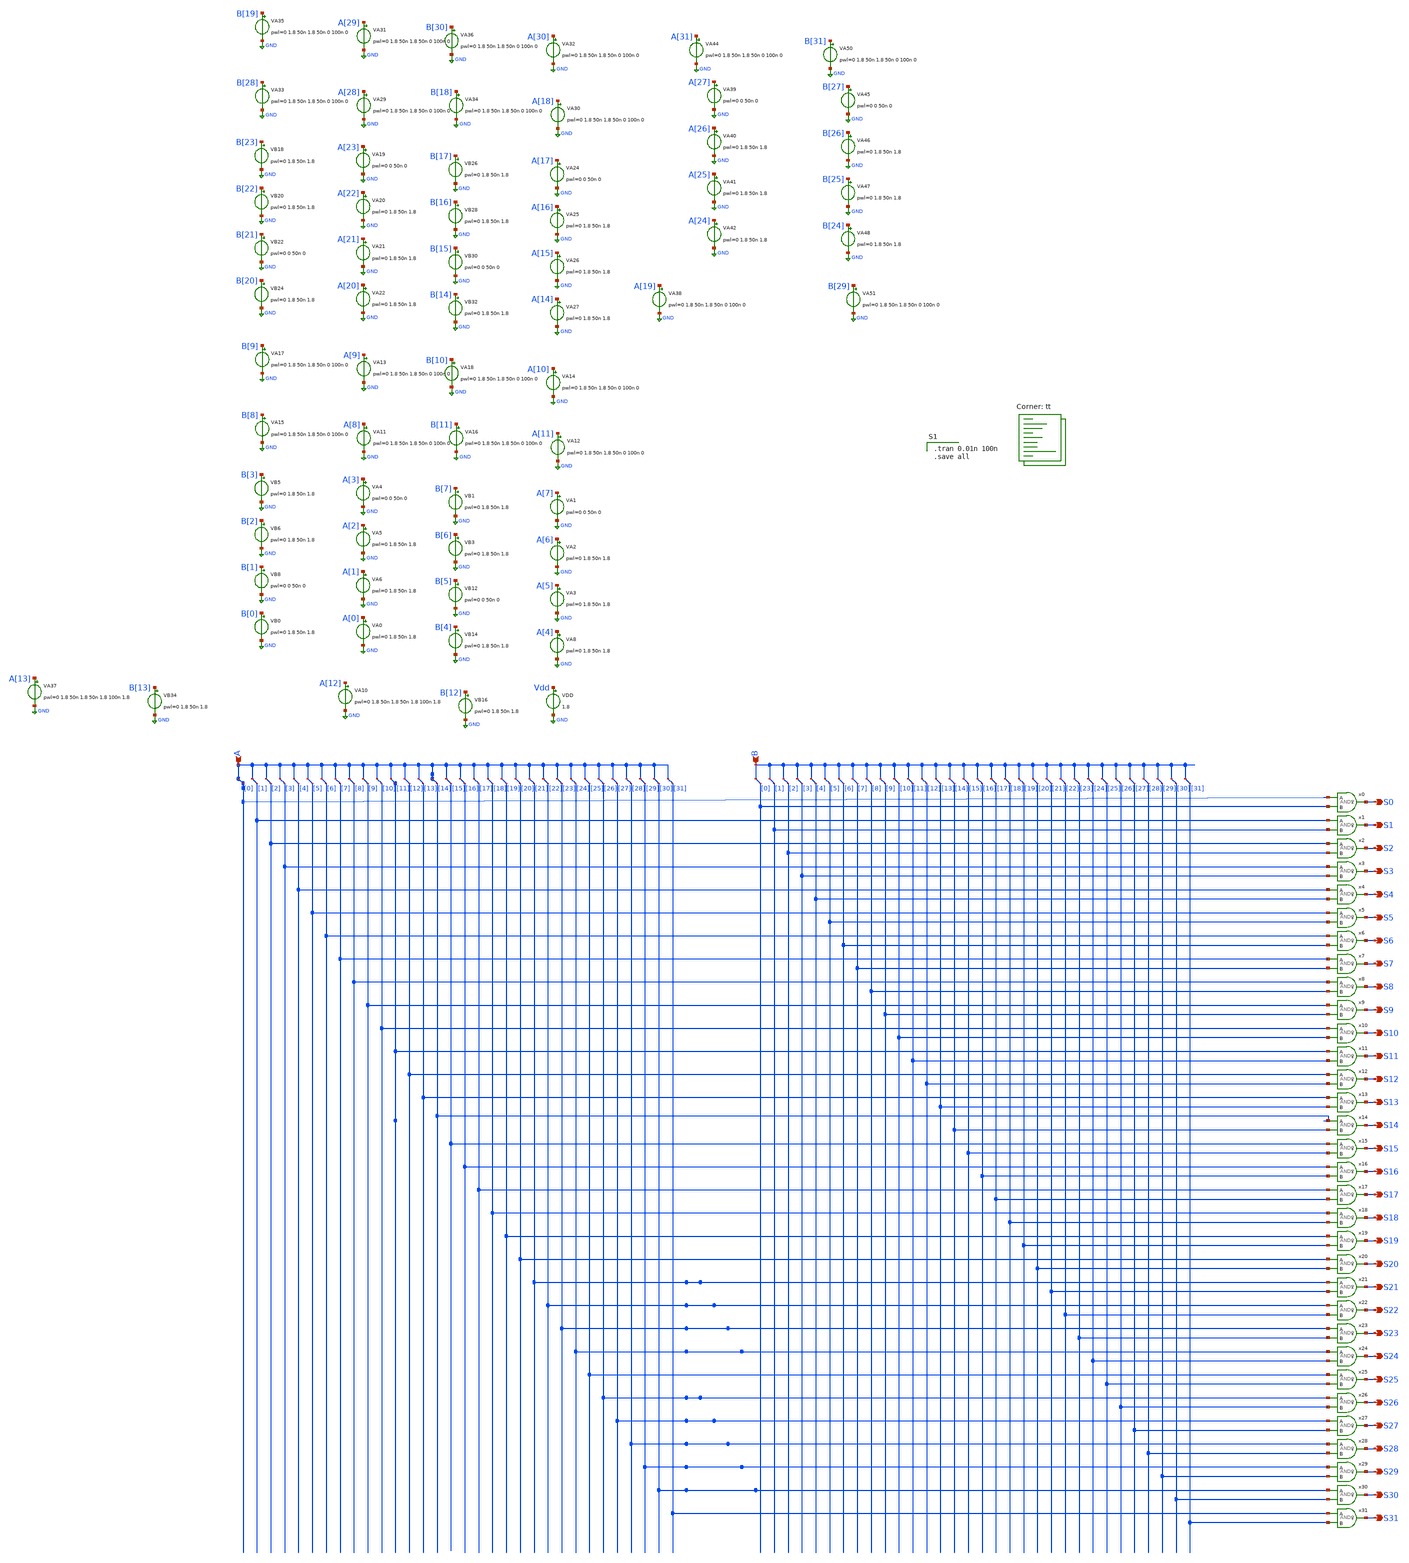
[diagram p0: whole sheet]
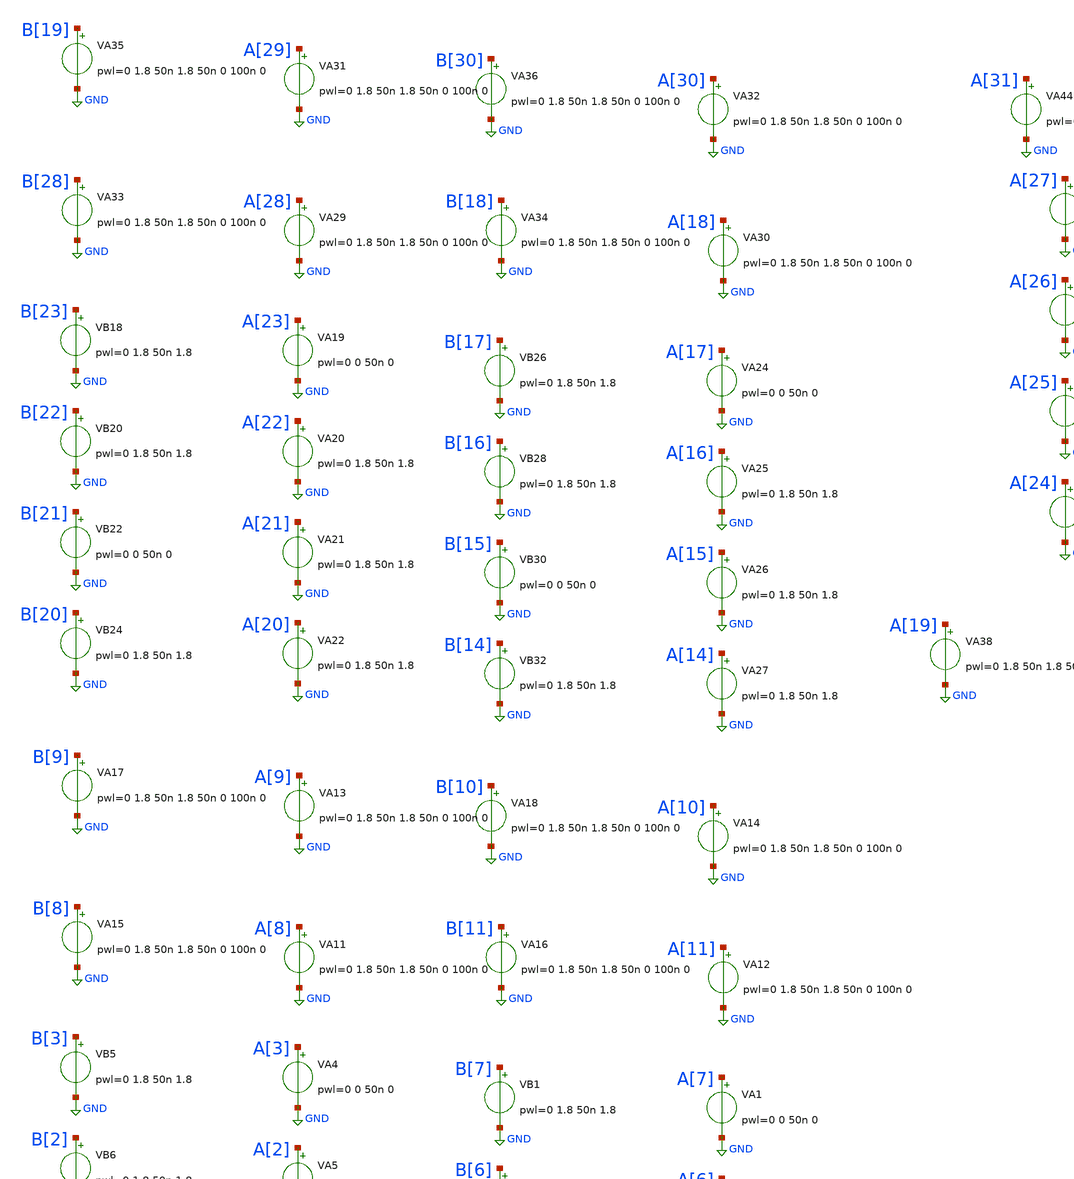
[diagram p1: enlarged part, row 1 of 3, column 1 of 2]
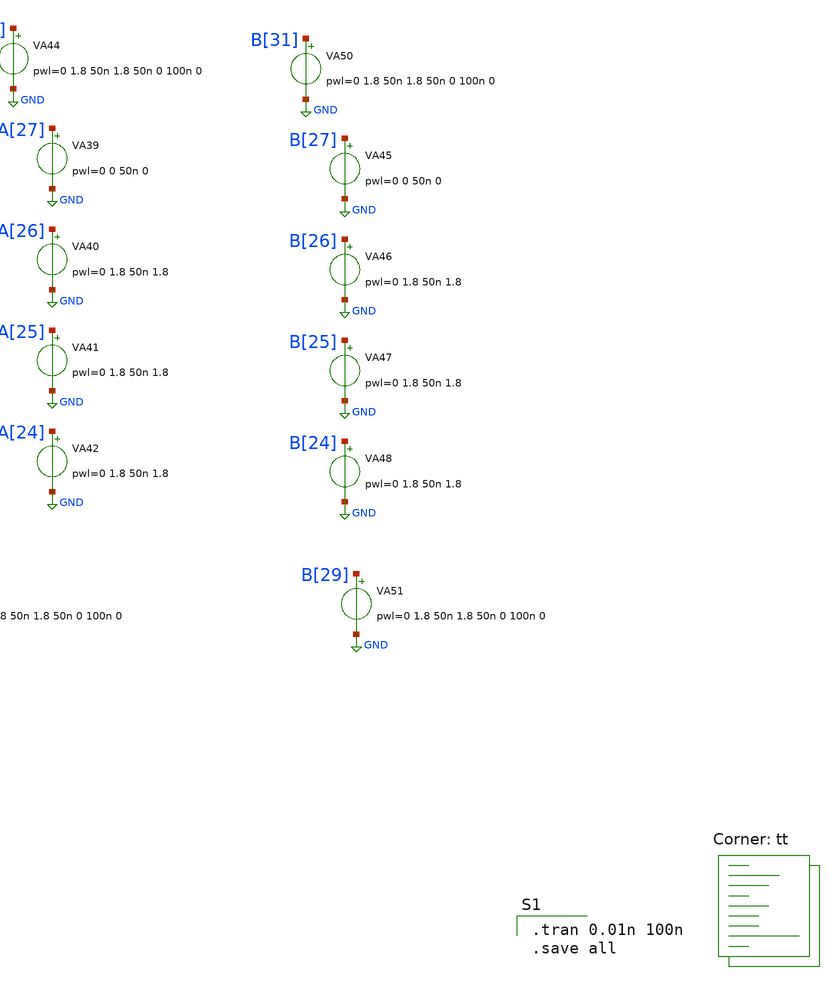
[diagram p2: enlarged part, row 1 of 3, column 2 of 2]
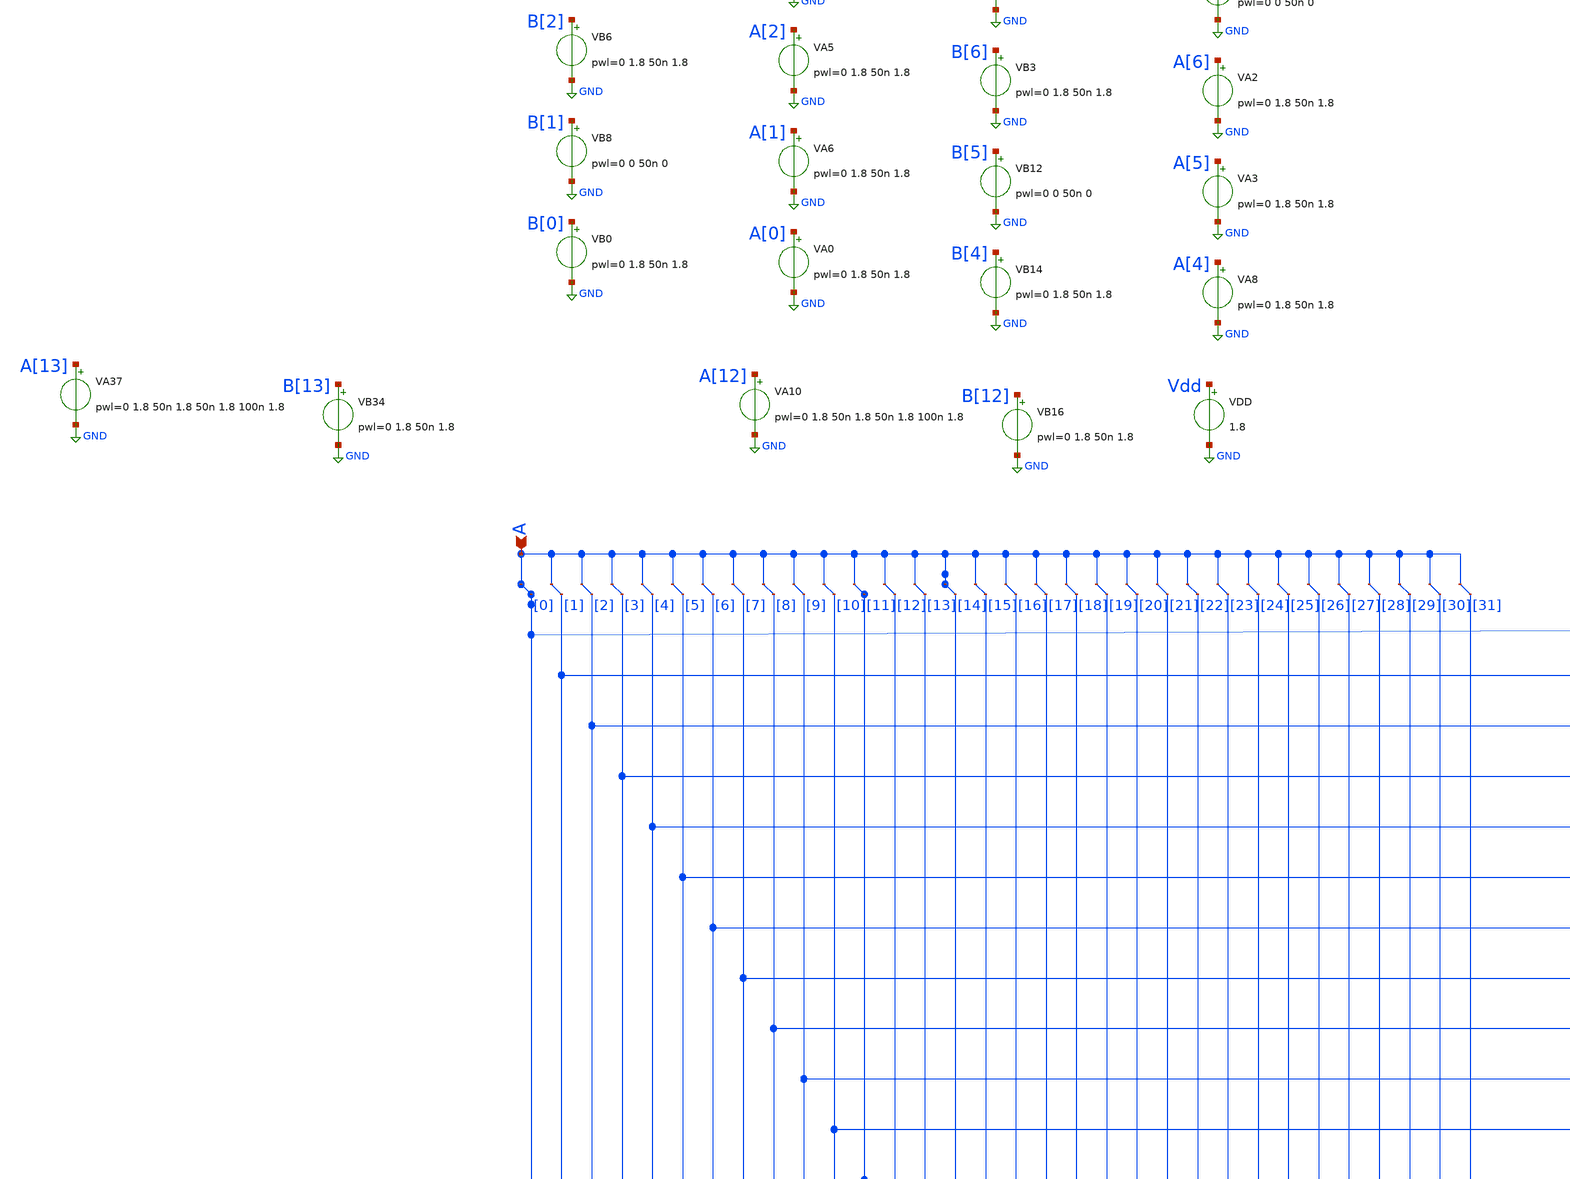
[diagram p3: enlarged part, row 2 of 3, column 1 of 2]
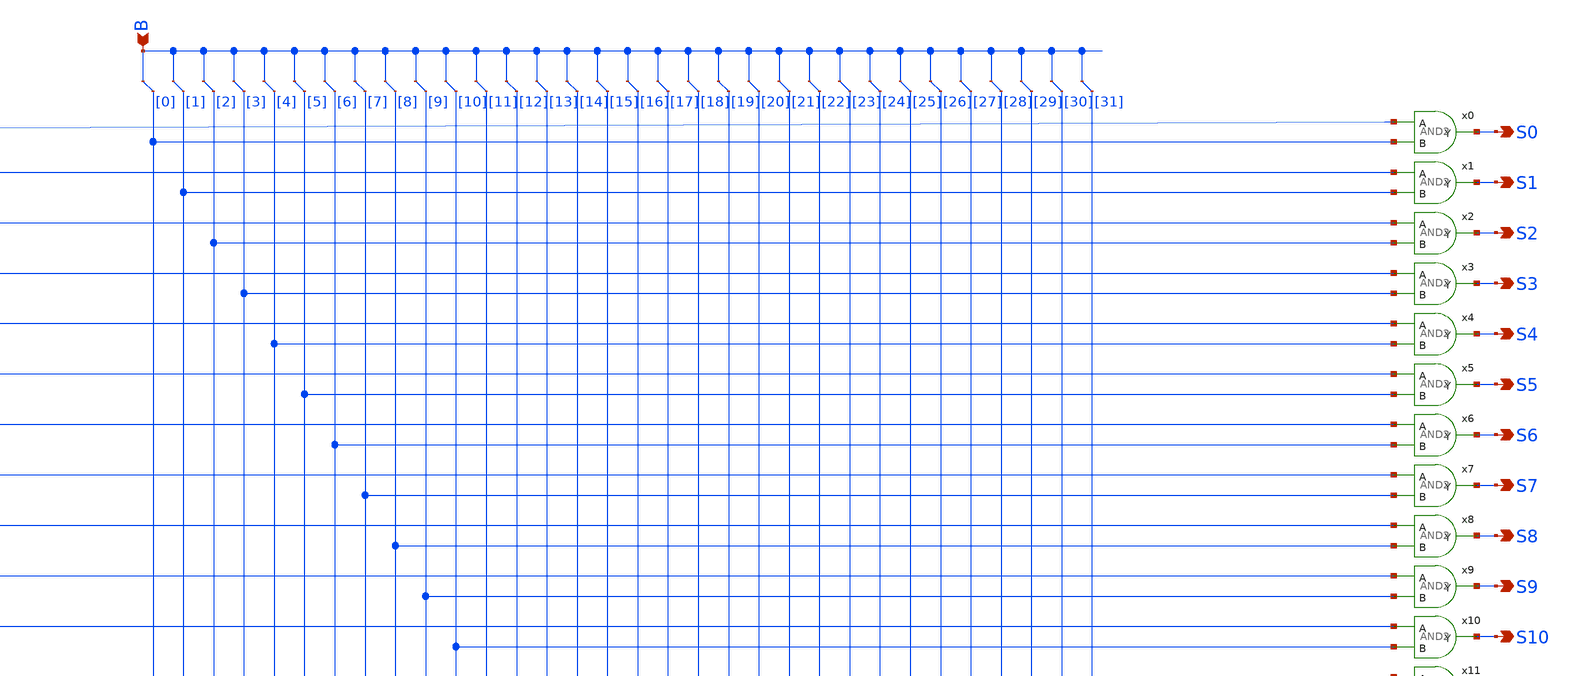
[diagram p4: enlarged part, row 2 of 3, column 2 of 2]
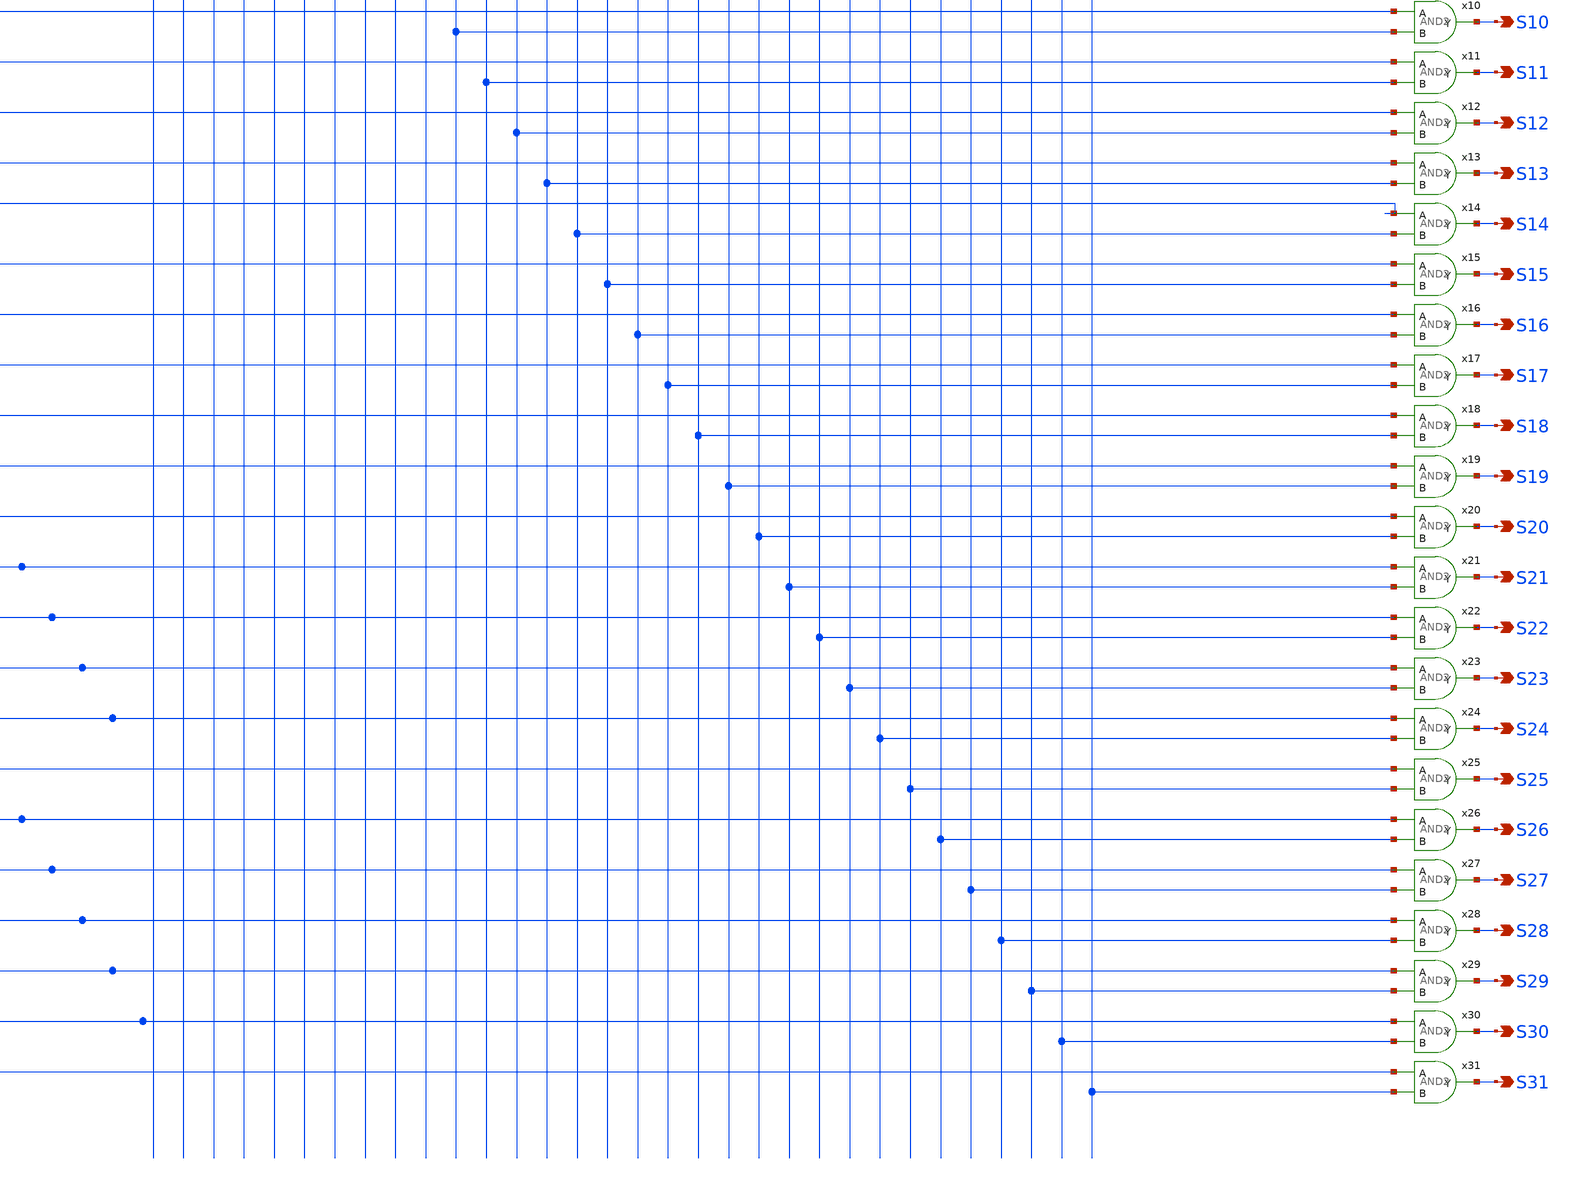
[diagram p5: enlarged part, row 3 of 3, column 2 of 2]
** sch_path: gates/32bit_ANDsim.sch
**.subckt 32bit_ANDsim S4 S5 S6 S7 S8 S9 S10 S11 S12 S13 S14 S15 S16 S17 S18 S19 S20 S21 S22 S23 S24
*+ S25 S26 S27 S28 S29 S30 S31 S0 S1 S2 S3 A B
*.opin S4
*.opin S5
*.opin S6
*.opin S7
*.opin S8
*.opin S9
*.opin S10
*.opin S11
*.opin S12
*.opin S13
*.opin S14
*.opin S15
*.opin S16
*.opin S17
*.opin S18
*.opin S19
*.opin S20
*.opin S21
*.opin S22
*.opin S23
*.opin S24
*.opin S25
*.opin S26
*.opin S27
*.opin S28
*.opin S29
*.opin S30
*.opin S31
*.opin S0
*.opin S1
*.opin S2
*.opin S3
*.ipin A
*.ipin B
x0 A[0] S0 B[0] AND2
* tap: A --> A[0]
* tap: A --> A[1]
* tap: A --> A[2]
* tap: A --> A[3]
* tap: A --> A[4]
* tap: A --> A[5]
* tap: A --> A[6]
* tap: A --> A[7]
* tap: A --> A[8]
* tap: A --> A[9]
* tap: A --> A[10]
* tap: A --> A[11]
* tap: A --> A[12]
* tap: A --> A[13]
* tap: A --> A[14]
* tap: A --> A[15]
* tap: A --> A[16]
* tap: A --> A[17]
* tap: A --> A[18]
* tap: A --> A[19]
* tap: A --> A[20]
* tap: A --> A[21]
* tap: A --> A[22]
* tap: A --> A[23]
* tap: A --> A[24]
* tap: A --> A[25]
* tap: A --> A[26]
* tap: A --> A[27]
* tap: A --> A[28]
* tap: A --> A[29]
* tap: A --> A[30]
* tap: A --> A[31]
* tap: B --> B[0]
* tap: B --> B[1]
* tap: B --> B[2]
* tap: B --> B[3]
* tap: B --> B[4]
* tap: B --> B[5]
* tap: B --> B[6]
* tap: B --> B[7]
* tap: B --> B[8]
* tap: B --> B[9]
* tap: B --> B[10]
* tap: B --> B[11]
* tap: B --> B[12]
* tap: B --> B[13]
* tap: B --> B[14]
* tap: B --> B[15]
* tap: B --> B[16]
* tap: B --> B[17]
* tap: B --> B[18]
* tap: B --> B[19]
* tap: B --> B[20]
* tap: B --> B[21]
* tap: B --> B[22]
* tap: B --> B[23]
* tap: B --> B[24]
* tap: B --> B[25]
* tap: B --> B[26]
* tap: B --> B[27]
* tap: B --> B[28]
* tap: B --> B[29]
* tap: B --> B[30]
* tap: B --> B[31]
x1 A[1] S1 B[1] AND2
x2 A[2] S2 B[2] AND2
x3 A[3] S3 B[3] AND2
x4 A[4] S4 B[4] AND2
x5 A[5] S5 B[5] AND2
x6 A[6] S6 B[6] AND2
x8 A[8] S8 B[8] AND2
x9 A[9] S9 B[9] AND2
x10 A[10] S10 B[10] AND2
x11 A[11] S11 B[11] AND2
x12 A[12] S12 B[12] AND2
x13 A[13] S13 B[13] AND2
x14 A[14] S14 B[14] AND2
x15 A[15] S15 B[15] AND2
x16 A[16] S16 B[16] AND2
x17 A[17] S17 B[17] AND2
x18 A[18] S18 B[18] AND2
x19 A[19] S19 B[19] AND2
x20 A[20] S20 B[20] AND2
x21 A[21] S21 B[21] AND2
x22 A[22] S22 B[22] AND2
x23 A[23] S23 B[23] AND2
x24 A[24] S24 B[24] AND2
x25 A[25] S25 B[25] AND2
x26 A[26] S26 B[26] AND2
x27 A[27] S27 B[27] AND2
x28 A[28] S28 B[28] AND2
x29 A[29] S29 B[29] AND2
x30 A[30] S30 B[30] AND2
x31 A[31] S31 B[31] AND2
x7 A[7] S7 B[7] AND2
VA10 A[12] GND pwl=0 1.8 50n 1.8 50n 1.8 100n 1.8
VB16 B[12] GND pwl=0 1.8 50n 1.8
VDD Vdd GND 1.8
VA4 A[3] GND pwl=0 0 50n 0
VA5 A[2] GND pwl=0 1.8 50n 1.8
VA6 A[1] GND pwl=0 1.8 50n 1.8
VA0 A[0] GND pwl=0 1.8 50n 1.8
VB5 B[3] GND pwl=0 1.8 50n 1.8
VB6 B[2] GND pwl=0 1.8 50n 1.8
VB8 B[1] GND pwl=0 0 50n 0
VB0 B[0] GND pwl=0 1.8 50n 1.8
VA1 A[7] GND pwl=0 0 50n 0
VA2 A[6] GND pwl=0 1.8 50n 1.8
VA3 A[5] GND pwl=0 1.8 50n 1.8
VA8 A[4] GND pwl=0 1.8 50n 1.8
VB1 B[7] GND pwl=0 1.8 50n 1.8
VB3 B[6] GND pwl=0 1.8 50n 1.8
VB12 B[5] GND pwl=0 0 50n 0
VB14 B[4] GND pwl=0 1.8 50n 1.8
VA11 A[8] GND pwl=0 1.8 50n 1.8 50n 0 100n 0
VA12 A[11] GND pwl=0 1.8 50n 1.8 50n 0 100n 0
VA13 A[9] GND pwl=0 1.8 50n 1.8 50n 0 100n 0
VA14 A[10] GND pwl=0 1.8 50n 1.8 50n 0 100n 0
VA15 B[8] GND pwl=0 1.8 50n 1.8 50n 0 100n 0
VA16 B[11] GND pwl=0 1.8 50n 1.8 50n 0 100n 0
VA17 B[9] GND pwl=0 1.8 50n 1.8 50n 0 100n 0
VA18 B[10] GND pwl=0 1.8 50n 1.8 50n 0 100n 0
VA19 A[23] GND pwl=0 0 50n 0
VA20 A[22] GND pwl=0 1.8 50n 1.8
VA21 A[21] GND pwl=0 1.8 50n 1.8
VA22 A[20] GND pwl=0 1.8 50n 1.8
VB18 B[23] GND pwl=0 1.8 50n 1.8
VB20 B[22] GND pwl=0 1.8 50n 1.8
VB22 B[21] GND pwl=0 0 50n 0
VB24 B[20] GND pwl=0 1.8 50n 1.8
VA24 A[17] GND pwl=0 0 50n 0
VA25 A[16] GND pwl=0 1.8 50n 1.8
VA26 A[15] GND pwl=0 1.8 50n 1.8
VA27 A[14] GND pwl=0 1.8 50n 1.8
VB26 B[17] GND pwl=0 1.8 50n 1.8
VB28 B[16] GND pwl=0 1.8 50n 1.8
VB30 B[15] GND pwl=0 0 50n 0
VB32 B[14] GND pwl=0 1.8 50n 1.8
VA29 A[28] GND pwl=0 1.8 50n 1.8 50n 0 100n 0
VA30 A[18] GND pwl=0 1.8 50n 1.8 50n 0 100n 0
VA31 A[29] GND pwl=0 1.8 50n 1.8 50n 0 100n 0
VA32 A[30] GND pwl=0 1.8 50n 1.8 50n 0 100n 0
VA33 B[28] GND pwl=0 1.8 50n 1.8 50n 0 100n 0
VA34 B[18] GND pwl=0 1.8 50n 1.8 50n 0 100n 0
VA35 B[19] GND pwl=0 1.8 50n 1.8 50n 0 100n 0
VA36 B[30] GND pwl=0 1.8 50n 1.8 50n 0 100n 0
VA37 A[13] GND pwl=0 1.8 50n 1.8 50n 1.8 100n 1.8
VB34 B[13] GND pwl=0 1.8 50n 1.8
VA38 A[19] GND pwl=0 1.8 50n 1.8 50n 0 100n 0
VA39 A[27] GND pwl=0 0 50n 0
VA40 A[26] GND pwl=0 1.8 50n 1.8
VA41 A[25] GND pwl=0 1.8 50n 1.8
VA42 A[24] GND pwl=0 1.8 50n 1.8
VA44 A[31] GND pwl=0 1.8 50n 1.8 50n 0 100n 0
VA45 B[27] GND pwl=0 0 50n 0
VA46 B[26] GND pwl=0 1.8 50n 1.8
VA47 B[25] GND pwl=0 1.8 50n 1.8
VA48 B[24] GND pwl=0 1.8 50n 1.8
VA50 B[31] GND pwl=0 1.8 50n 1.8 50n 0 100n 0
VA51 B[29] GND pwl=0 1.8 50n 1.8 50n 0 100n 0
**** begin user architecture code

.tran 0.01n 100n
.save all

.lib $::SKYWATER_MODELS/sky130.lib.spice tt
**** end user architecture code
**.ends

* expanding   symbol:  AND2.sym # of pins=3
** sym_path: gates/AND2.sym
** sch_path: gates/AND2.sch
.subckt AND2 A Y B
*.opin Y
*.ipin A
*.ipin B
x1 A net1 B NAND2_Gate
X2 net1 Y inv_vtc
.ends


* expanding   symbol:  NAND2_Gate.sym # of pins=3
** sym_path: gates/NAND2_Gate.sym
** sch_path: gates/NAND2_Gate.sch
.subckt NAND2_Gate A Y B
*.ipin A
*.ipin B
*.opin Y
XM1 Y A net1 GND sky130_fd_pr__nfet_01v8 L=0.15 W=1 nf=1 ad='int((nf+1)/2) * W/nf * 0.29' as='int((nf+2)/2) * W/nf * 0.29'
+ pd='2*int((nf+1)/2) * (W/nf + 0.29)' ps='2*int((nf+2)/2) * (W/nf + 0.29)' nrd='0.29 / W' nrs='0.29 / W'
+ sa=0 sb=0 sd=0 mult=1 m=1
XM2 net1 B GND GND sky130_fd_pr__nfet_01v8 L=0.15 W=1 nf=1 ad='int((nf+1)/2) * W/nf * 0.29' as='int((nf+2)/2) * W/nf * 0.29'
+ pd='2*int((nf+1)/2) * (W/nf + 0.29)' ps='2*int((nf+2)/2) * (W/nf + 0.29)' nrd='0.29 / W' nrs='0.29 / W'
+ sa=0 sb=0 sd=0 mult=1 m=1
XM3 Y A VDD VDD sky130_fd_pr__pfet_01v8 L=0.15 W=1 nf=1 ad='int((nf+1)/2) * W/nf * 0.29' as='int((nf+2)/2) * W/nf * 0.29'
+ pd='2*int((nf+1)/2) * (W/nf + 0.29)' ps='2*int((nf+2)/2) * (W/nf + 0.29)' nrd='0.29 / W' nrs='0.29 / W'
+ sa=0 sb=0 sd=0 mult=1 m=1
XM4 Y B VDD VDD sky130_fd_pr__pfet_01v8 L=0.15 W=1 nf=1 ad='int((nf+1)/2) * W/nf * 0.29' as='int((nf+2)/2) * W/nf * 0.29'
+ pd='2*int((nf+1)/2) * (W/nf + 0.29)' ps='2*int((nf+2)/2) * (W/nf + 0.29)' nrd='0.29 / W' nrs='0.29 / W'
+ sa=0 sb=0 sd=0 mult=1 m=1
.ends


* expanding   symbol:  /home/apn/test_xschem_sky130/inv_vtc.sym # of pins=2
** sym_path: gates/inv_vtc.sym
** sch_path: gates/inv_vtc.sch
.subckt inv_vtc A Y
*.ipin A
*.opin Y
XM1 Y A VDD VDD sky130_fd_pr__pfet_01v8 L=0.15 W=2 nf=1 ad='int((nf+1)/2) * W/nf * 0.29' as='int((nf+2)/2) * W/nf * 0.29'
+ pd='2*int((nf+1)/2) * (W/nf + 0.29)' ps='2*int((nf+2)/2) * (W/nf + 0.29)' nrd='0.29 / W' nrs='0.29 / W'
+ sa=0 sb=0 sd=0 mult=1 m=1
XM2 Y A GND GND sky130_fd_pr__nfet_01v8 L=0.15 W=1 nf=1 ad='int((nf+1)/2) * W/nf * 0.29' as='int((nf+2)/2) * W/nf * 0.29'
+ pd='2*int((nf+1)/2) * (W/nf + 0.29)' ps='2*int((nf+2)/2) * (W/nf + 0.29)' nrd='0.29 / W' nrs='0.29 / W'
+ sa=0 sb=0 sd=0 mult=1 m=1
.ends

.GLOBAL GND
.GLOBAL VDD
.end
